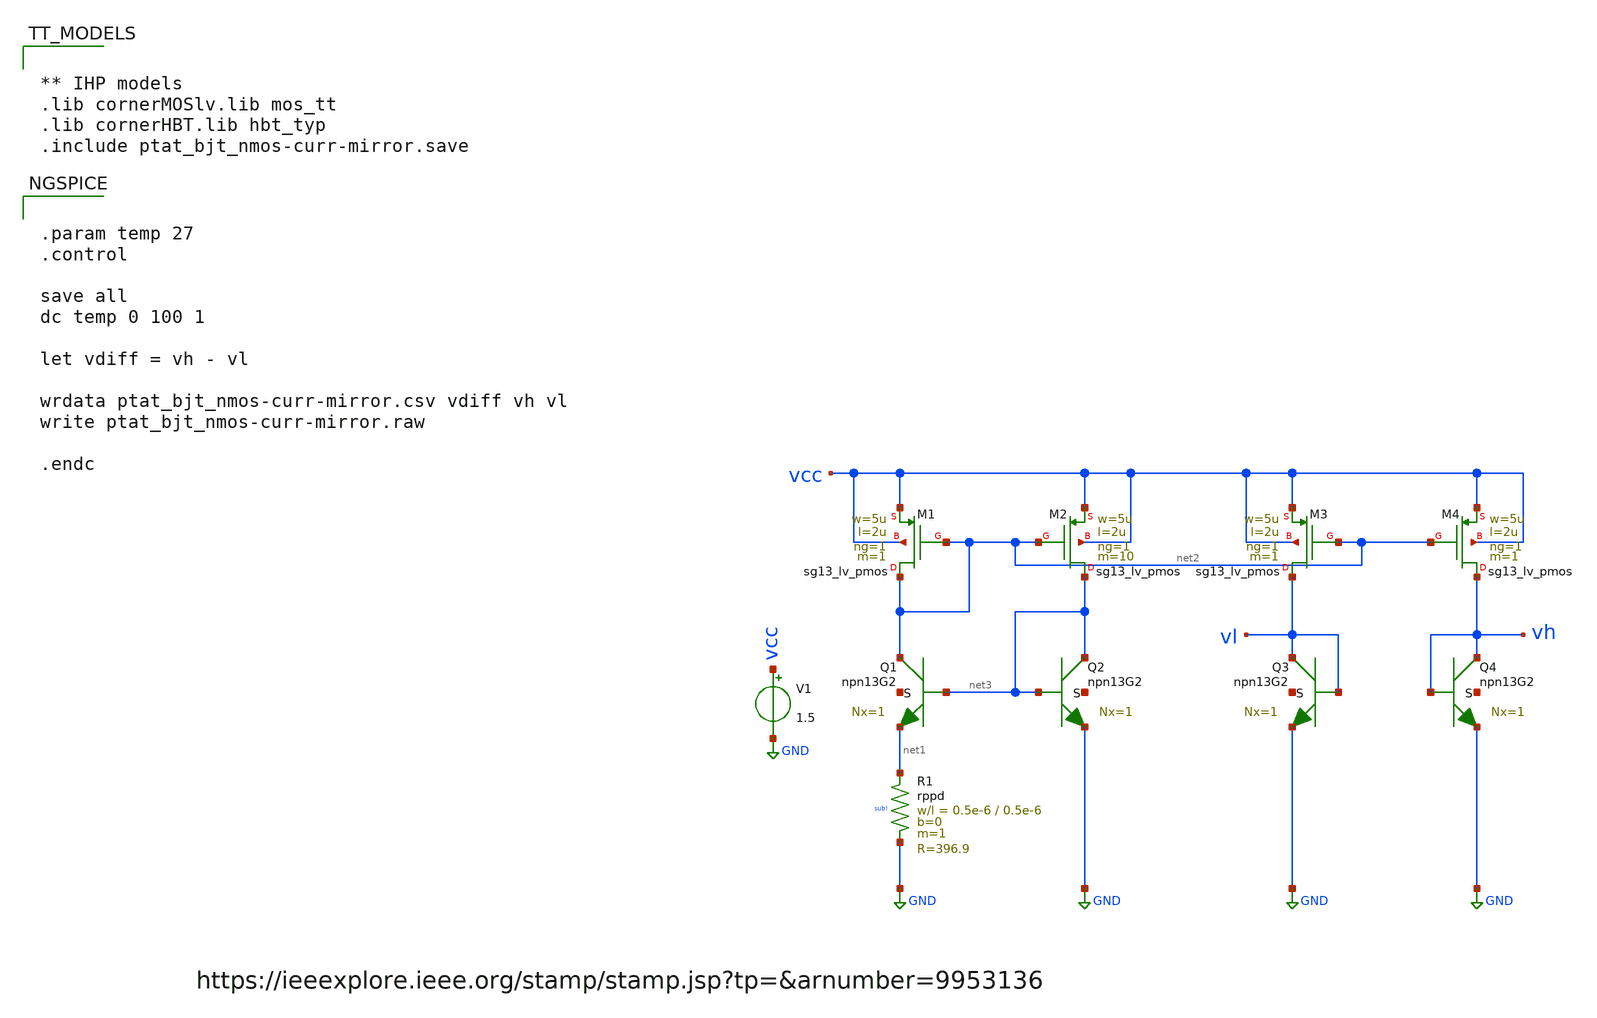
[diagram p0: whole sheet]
** sch_path: TempSensor/design_data/xschem/a-210nW-npn-based-temp-sens.sch
**.subckt a-210nW-npn-based-temp-sens
XM1 net2 net2 vcc vcc sg13_lv_pmos w=5u l=2u ng=1 m=1 mm_ok=1
XM2 net3 net2 vcc vcc sg13_lv_pmos w=5u l=2u ng=1 m=10 mm_ok=1
XM3 vl net2 vcc vcc sg13_lv_pmos w=5u l=2u ng=1 m=1 mm_ok=1
XM4 vh net2 vcc vcc sg13_lv_pmos w=5u l=2u ng=1 m=1 mm_ok=1
XQ1 net2 net3 net1 net4 npn13G2 Nx=1 mm_ok=1
XQ2 net3 net3 GND net5 npn13G2 Nx=1 mm_ok=1
XQ3 vl vl GND net6 npn13G2 Nx=1 mm_ok=1
XQ4 vh vh GND net7 npn13G2 Nx=1 mm_ok=1
XR1 net1 GND sub! rppd w=0.5e-6 l=0.5e-6 m=1 b=0 mm_ok=1
V1 vcc GND 1.5
**** begin user architecture code


.param temp 27
.control

save all
dc temp 0 100 1

let vdiff = vh - vl

wrdata ptat_bjt_nmos-curr-mirror.csv vdiff vh vl
write ptat_bjt_nmos-curr-mirror.raw

.endc




** IHP models
.lib cornerMOSlv.lib mos_tt
.lib cornerHBT.lib hbt_typ
.include ptat_bjt_nmos-curr-mirror.save


**** end user architecture code
**.ends
.GLOBAL GND
.end
